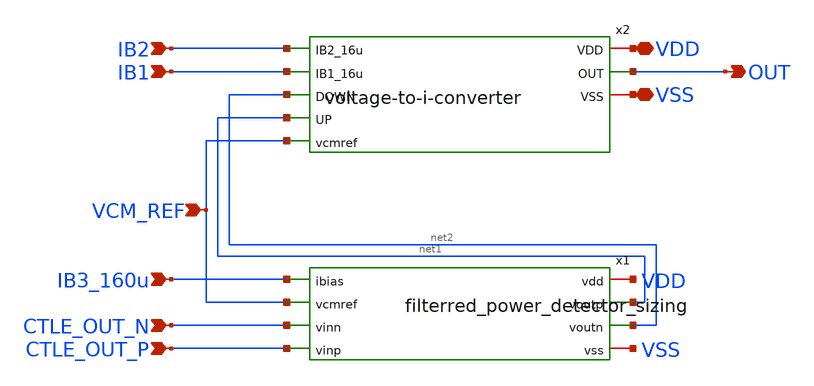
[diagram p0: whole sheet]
** sch_path: pd-converter/vctrl-generator.sch
**.subckt vctrl-generator IB1 IB2 IB3_160u VDD VSS OUT CTLE_OUT_N CTLE_OUT_P VCM_REF
*.ipin IB1
*.ipin IB2
*.ipin IB3_160u
*.iopin VDD
*.iopin VSS
*.opin OUT
*.ipin CTLE_OUT_N
*.ipin CTLE_OUT_P
*.ipin VCM_REF
x1 VDD net1 net2 IB3_160u VSS VCM_REF CTLE_OUT_N CTLE_OUT_P filterred_power_detector_sizing
x2 VDD IB2 IB1 OUT net2 net1 VCM_REF VSS voltage-to-i-converter
**.ends

* expanding   symbol:
*+  /foss/designs/afe-icdec-teknofest-2026/CTLE/filterred_power_detector_sizing.sym # of pins=8
** sym_path: CTLE/filterred_power_detector_sizing.sym
** sch_path: CTLE/filterred_power_detector_sizing.sch
.subckt filterred_power_detector_sizing vdd voutp voutn ibias vss vcmref vinn vinp
*.ipin vinp
*.ipin vinn
*.opin voutp
*.opin voutn
*.ipin ibias
*.iopin vss
*.iopin vdd
*.ipin vcmref
XM1 voutp Vhf_pos net1 vss sky130_fd_pr__nfet_01v8 L=0.45 W=1.23 nf=1 ad='int((nf+1)/2) * W/nf * 0.29'
+ as='int((nf+2)/2) * W/nf * 0.29' pd='2*int((nf+1)/2) * (W/nf + 0.29)' ps='2*int((nf+2)/2) * (W/nf + 0.29)'
+ nrd='0.29 / W' nrs='0.29 / W' sa=0 sb=0 sd=0 mult=1 m=1
XM2 voutp Vhf_neg net1 vss sky130_fd_pr__nfet_01v8 L=0.45 W=1.23 nf=1 ad='int((nf+1)/2) * W/nf * 0.29'
+ as='int((nf+2)/2) * W/nf * 0.29' pd='2*int((nf+1)/2) * (W/nf + 0.29)' ps='2*int((nf+2)/2) * (W/nf + 0.29)'
+ nrd='0.29 / W' nrs='0.29 / W' sa=0 sb=0 sd=0 mult=1 m=1
XM3 voutn Vlf_pos net1 vss sky130_fd_pr__nfet_01v8 L=0.75 W=1.23 nf=1 ad='int((nf+1)/2) * W/nf * 0.29'
+ as='int((nf+2)/2) * W/nf * 0.29' pd='2*int((nf+1)/2) * (W/nf + 0.29)' ps='2*int((nf+2)/2) * (W/nf + 0.29)'
+ nrd='0.29 / W' nrs='0.29 / W' sa=0 sb=0 sd=0 mult=1 m=1
XM4 voutn Vlf_neg net1 vss sky130_fd_pr__nfet_01v8 L=0.45 W=1.23 nf=1 ad='int((nf+1)/2) * W/nf * 0.29'
+ as='int((nf+2)/2) * W/nf * 0.29' pd='2*int((nf+1)/2) * (W/nf + 0.29)' ps='2*int((nf+2)/2) * (W/nf + 0.29)'
+ nrd='0.29 / W' nrs='0.29 / W' sa=0 sb=0 sd=0 mult=1 m=1
XC7 Vhf_neg vinn sky130_fd_pr__cap_mim_m3_1 W=5.7921 L=5.7921 MF=1 m=1
XC3 Vhf_pos vinp sky130_fd_pr__cap_mim_m3_1 W=5.7921 L=5.7921 MF=1 m=1
XR9 Vhf_neg net2 vss sky130_fd_pr__res_high_po_5p73 L=69.65 mult=4 m=4
XR3 net2 Vhf_pos vss sky130_fd_pr__res_high_po_5p73 L=69.65 mult=4 m=4
XR4 vcmref vinn vss sky130_fd_pr__res_high_po_5p73 L=708 mult=4 m=4
XR5 vinp vcmref vss sky130_fd_pr__res_high_po_5p73 L=708 mult=4 m=4
XC4 net2 vss sky130_fd_pr__cap_mim_m3_1 W=0.4208 L=0.4208 MF=1 m=1
XR6 Vlf_pos vinp vss sky130_fd_pr__res_high_po_5p73 L=69.65 mult=4 m=4
XR7 vinn Vlf_neg vss sky130_fd_pr__res_high_po_5p73 L=69.65 mult=4 m=4
XC2 Vlf_pos vss sky130_fd_pr__cap_mim_m3_1 W=5.7921 L=5.7921 MF=1 m=1
XC5 vss Vlf_neg sky130_fd_pr__cap_mim_m3_1 W=5.7921 L=5.7921 MF=1 m=1
XC6 voutp voutn sky130_fd_pr__cap_mim_m3_1 W=0.2019 L=0.2019 MF=1 m=1
XR8 voutp vdd vss sky130_fd_pr__res_high_po_5p73 L=796.338 mult=4 m=4
XR1 voutn vdd vss sky130_fd_pr__res_high_po_5p73 L=796.338 mult=4 m=4
XM5 net1 ibias vss vss sky130_fd_pr__nfet_01v8 L=0.45 W=4.92 nf=1 ad='int((nf+1)/2) * W/nf * 0.29' as='int((nf+2)/2) * W/nf * 0.29'
+ pd='2*int((nf+1)/2) * (W/nf + 0.29)' ps='2*int((nf+2)/2) * (W/nf + 0.29)' nrd='0.29 / W' nrs='0.29 / W'
+ sa=0 sb=0 sd=0 mult=1 m=1
XM6 ibias ibias vss vss sky130_fd_pr__nfet_01v8 L=0.45 W=0.45 nf=1 ad='int((nf+1)/2) * W/nf * 0.29' as='int((nf+2)/2) * W/nf * 0.29'
+ pd='2*int((nf+1)/2) * (W/nf + 0.29)' ps='2*int((nf+2)/2) * (W/nf + 0.29)' nrd='0.29 / W' nrs='0.29 / W'
+ sa=0 sb=0 sd=0 mult=1 m=1
.ends


* expanding   symbol:  /foss/designs/afe-icdec-teknofest-2026/CTLE/voltage-to-i-converter.sym # of
*+ pins=8
** sym_path: CTLE/voltage-to-i-converter.sym
** sch_path: CTLE/voltage-to-i-converter.sch
.subckt voltage-to-i-converter VDD IB2_16u IB1_16u OUT DOWN UP vcmref VSS
*.iopin VDD
*.iopin VSS
*.opin OUT
*.ipin IB2_16u
*.ipin UP
*.ipin DOWN
*.ipin IB1_16u
*.ipin vcmref
XM1 net3 net3 VDD VDD sky130_fd_pr__pfet_01v8 L=0.6 W=75 nf=1 ad='int((nf+1)/2) * W/nf * 0.29' as='int((nf+2)/2) * W/nf * 0.29'
+ pd='2*int((nf+1)/2) * (W/nf + 0.29)' ps='2*int((nf+2)/2) * (W/nf + 0.29)' nrd='0.29 / W' nrs='0.29 / W'
+ sa=0 sb=0 sd=0 mult=1 m=1
XM2 net5 net5 VDD VDD sky130_fd_pr__pfet_01v8 L=0.6 W=75 nf=1 ad='int((nf+1)/2) * W/nf * 0.29' as='int((nf+2)/2) * W/nf * 0.29'
+ pd='2*int((nf+1)/2) * (W/nf + 0.29)' ps='2*int((nf+2)/2) * (W/nf + 0.29)' nrd='0.29 / W' nrs='0.29 / W'
+ sa=0 sb=0 sd=0 mult=1 m=1
XM5 net1 IB1_16u VSS VSS sky130_fd_pr__nfet_01v8 L=1.5 W=25 nf=1 ad='int((nf+1)/2) * W/nf * 0.29' as='int((nf+2)/2) * W/nf * 0.29'
+ pd='2*int((nf+1)/2) * (W/nf + 0.29)' ps='2*int((nf+2)/2) * (W/nf + 0.29)' nrd='0.29 / W' nrs='0.29 / W'
+ sa=0 sb=0 sd=0 mult=1 m=1
XM6 IB1_16u IB1_16u VSS VSS sky130_fd_pr__nfet_01v8 L=1.5 W=25 nf=1 ad='int((nf+1)/2) * W/nf * 0.29'
+ as='int((nf+2)/2) * W/nf * 0.29' pd='2*int((nf+1)/2) * (W/nf + 0.29)' ps='2*int((nf+2)/2) * (W/nf + 0.29)'
+ nrd='0.29 / W' nrs='0.29 / W' sa=0 sb=0 sd=0 mult=1 m=1
XM7 net4 net4 VDD VDD sky130_fd_pr__pfet_01v8 L=0.6 W=75 nf=1 ad='int((nf+1)/2) * W/nf * 0.29' as='int((nf+2)/2) * W/nf * 0.29'
+ pd='2*int((nf+1)/2) * (W/nf + 0.29)' ps='2*int((nf+2)/2) * (W/nf + 0.29)' nrd='0.29 / W' nrs='0.29 / W'
+ sa=0 sb=0 sd=0 mult=1 m=1
XM8 net6 net6 VDD VDD sky130_fd_pr__pfet_01v8 L=0.6 W=75 nf=1 ad='int((nf+1)/2) * W/nf * 0.29' as='int((nf+2)/2) * W/nf * 0.29'
+ pd='2*int((nf+1)/2) * (W/nf + 0.29)' ps='2*int((nf+2)/2) * (W/nf + 0.29)' nrd='0.29 / W' nrs='0.29 / W'
+ sa=0 sb=0 sd=0 mult=1 m=1
XM11 net2 IB2_16u VSS VSS sky130_fd_pr__nfet_01v8 L=1.5 W=25 nf=1 ad='int((nf+1)/2) * W/nf * 0.29' as='int((nf+2)/2) * W/nf * 0.29'
+ pd='2*int((nf+1)/2) * (W/nf + 0.29)' ps='2*int((nf+2)/2) * (W/nf + 0.29)' nrd='0.29 / W' nrs='0.29 / W'
+ sa=0 sb=0 sd=0 mult=1 m=1
XM12 IB2_16u IB2_16u VSS VSS sky130_fd_pr__nfet_01v8 L=1.5 W=25 nf=1 ad='int((nf+1)/2) * W/nf * 0.29'
+ as='int((nf+2)/2) * W/nf * 0.29' pd='2*int((nf+1)/2) * (W/nf + 0.29)' ps='2*int((nf+2)/2) * (W/nf + 0.29)'
+ nrd='0.29 / W' nrs='0.29 / W' sa=0 sb=0 sd=0 mult=1 m=1
XM13 OUT net6 VDD VDD sky130_fd_pr__pfet_01v8 L=0.6 W=75 nf=1 ad='int((nf+1)/2) * W/nf * 0.29' as='int((nf+2)/2) * W/nf * 0.29'
+ pd='2*int((nf+1)/2) * (W/nf + 0.29)' ps='2*int((nf+2)/2) * (W/nf + 0.29)' nrd='0.29 / W' nrs='0.29 / W'
+ sa=0 sb=0 sd=0 mult=1 m=1
XM14 net7 net5 VDD VDD sky130_fd_pr__pfet_01v8 L=0.6 W=75 nf=1 ad='int((nf+1)/2) * W/nf * 0.29' as='int((nf+2)/2) * W/nf * 0.29'
+ pd='2*int((nf+1)/2) * (W/nf + 0.29)' ps='2*int((nf+2)/2) * (W/nf + 0.29)' nrd='0.29 / W' nrs='0.29 / W'
+ sa=0 sb=0 sd=0 mult=1 m=1
XM15 net7 net7 VSS VSS sky130_fd_pr__nfet_01v8 L=1.5 W=25 nf=1 ad='int((nf+1)/2) * W/nf * 0.29' as='int((nf+2)/2) * W/nf * 0.29'
+ pd='2*int((nf+1)/2) * (W/nf + 0.29)' ps='2*int((nf+2)/2) * (W/nf + 0.29)' nrd='0.29 / W' nrs='0.29 / W'
+ sa=0 sb=0 sd=0 mult=1 m=1
XM16 OUT net7 VSS VSS sky130_fd_pr__nfet_01v8 L=1.5 W=25 nf=1 ad='int((nf+1)/2) * W/nf * 0.29' as='int((nf+2)/2) * W/nf * 0.29'
+ pd='2*int((nf+1)/2) * (W/nf + 0.29)' ps='2*int((nf+2)/2) * (W/nf + 0.29)' nrd='0.29 / W' nrs='0.29 / W'
+ sa=0 sb=0 sd=0 mult=1 m=1
XR1 DOWN vcmref VSS sky130_fd_pr__res_high_po_0p35 L=50 mult=1 m=1
XR2 vcmref UP VSS sky130_fd_pr__res_high_po_0p35 L=50 mult=1 m=1
XC1 OUT VSS sky130_fd_pr__cap_mim_m3_1 W=30 L=30 MF=4 m=4
XM3 net5 DOWN net1 VSS sky130_fd_pr__nfet_01v8 L=0.5 W=25 nf=1 ad='int((nf+1)/2) * W/nf * 0.29' as='int((nf+2)/2) * W/nf * 0.29'
+ pd='2*int((nf+1)/2) * (W/nf + 0.29)' ps='2*int((nf+2)/2) * (W/nf + 0.29)' nrd='0.29 / W' nrs='0.29 / W'
+ sa=0 sb=0 sd=0 mult=1 m=1
XM4 net3 vcmref net1 VSS sky130_fd_pr__nfet_01v8 L=0.5 W=25 nf=1 ad='int((nf+1)/2) * W/nf * 0.29' as='int((nf+2)/2) * W/nf * 0.29'
+ pd='2*int((nf+1)/2) * (W/nf + 0.29)' ps='2*int((nf+2)/2) * (W/nf + 0.29)' nrd='0.29 / W' nrs='0.29 / W'
+ sa=0 sb=0 sd=0 mult=1 m=1
XM9 net4 vcmref net2 VSS sky130_fd_pr__nfet_01v8 L=0.5 W=25 nf=1 ad='int((nf+1)/2) * W/nf * 0.29' as='int((nf+2)/2) * W/nf * 0.29'
+ pd='2*int((nf+1)/2) * (W/nf + 0.29)' ps='2*int((nf+2)/2) * (W/nf + 0.29)' nrd='0.29 / W' nrs='0.29 / W'
+ sa=0 sb=0 sd=0 mult=1 m=1
XM10 net6 UP net2 VSS sky130_fd_pr__nfet_01v8 L=0.5 W=25 nf=1 ad='int((nf+1)/2) * W/nf * 0.29' as='int((nf+2)/2) * W/nf * 0.29'
+ pd='2*int((nf+1)/2) * (W/nf + 0.29)' ps='2*int((nf+2)/2) * (W/nf + 0.29)' nrd='0.29 / W' nrs='0.29 / W'
+ sa=0 sb=0 sd=0 mult=1 m=1
.ends

.end
